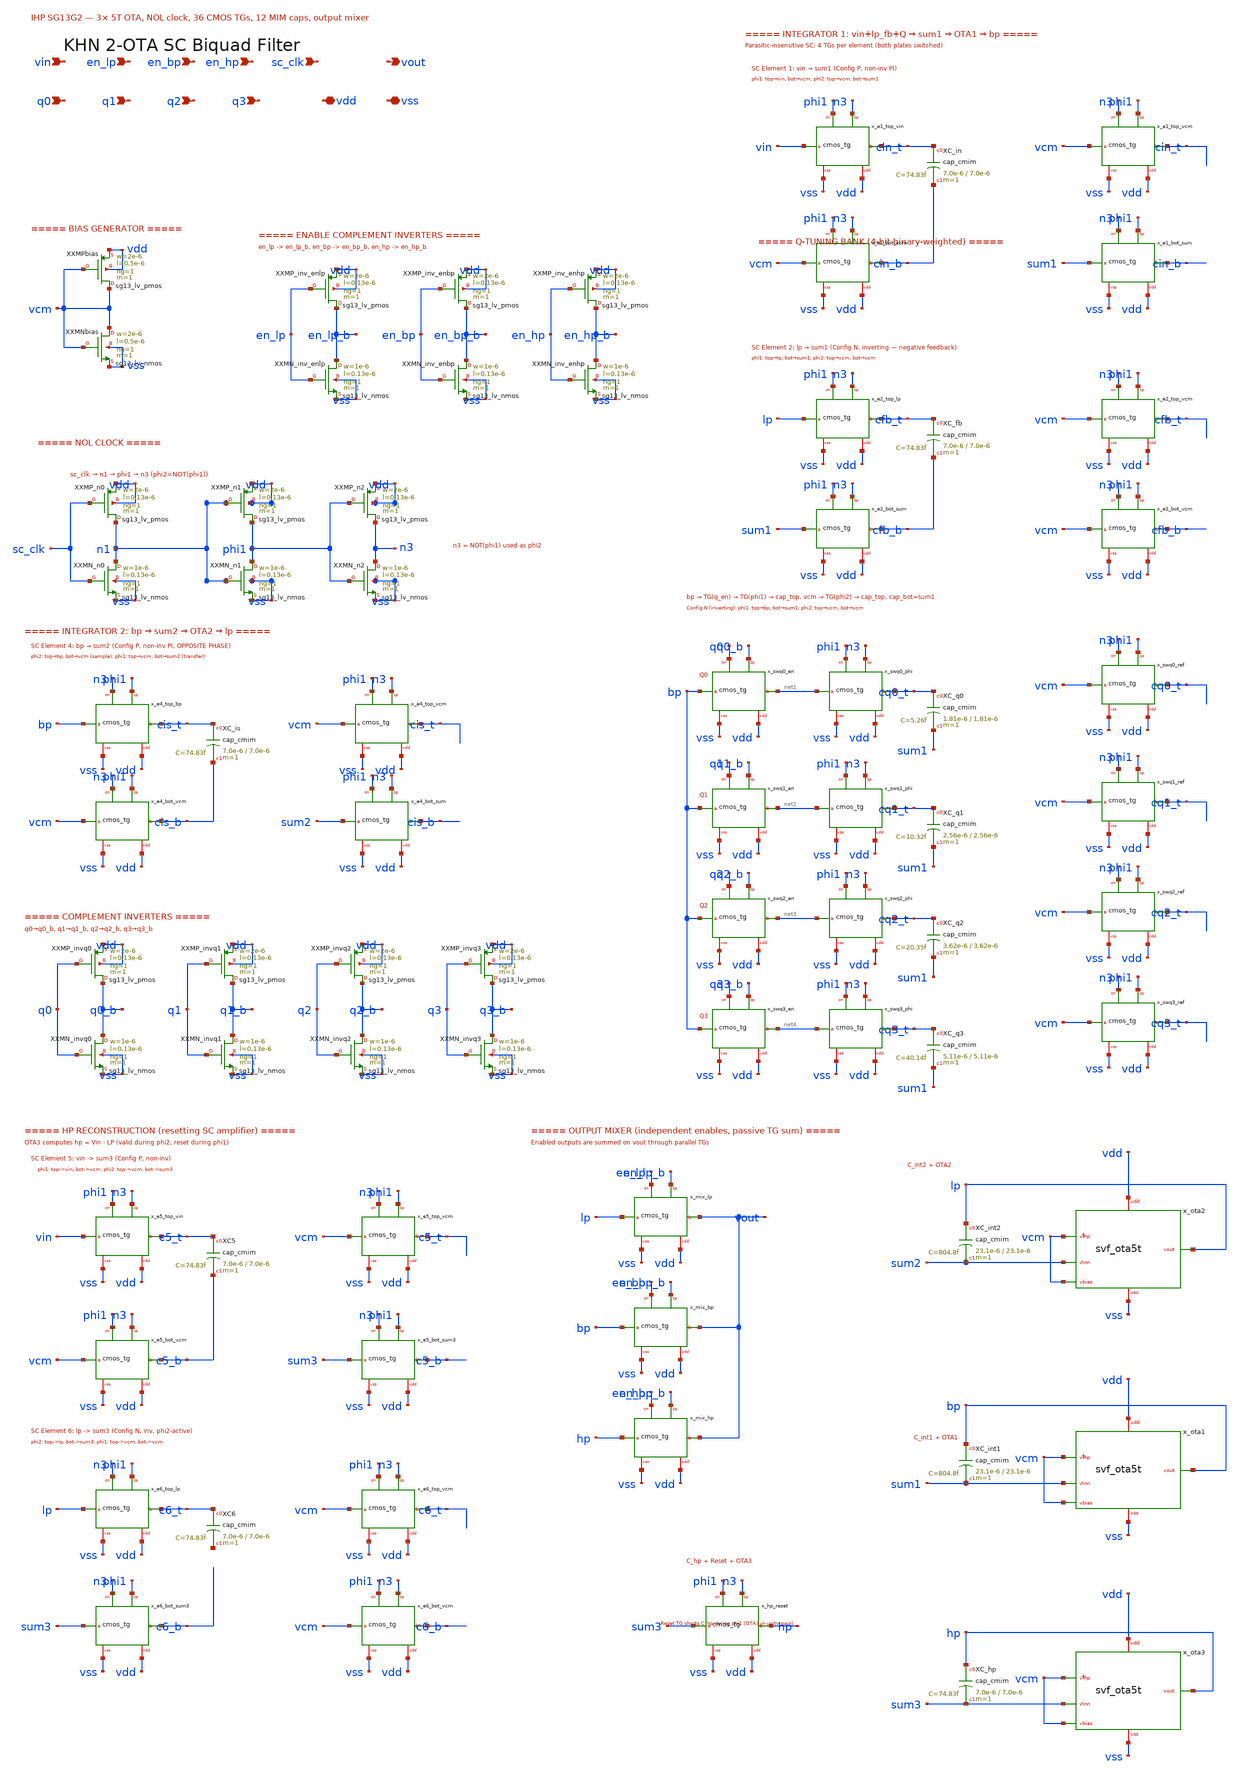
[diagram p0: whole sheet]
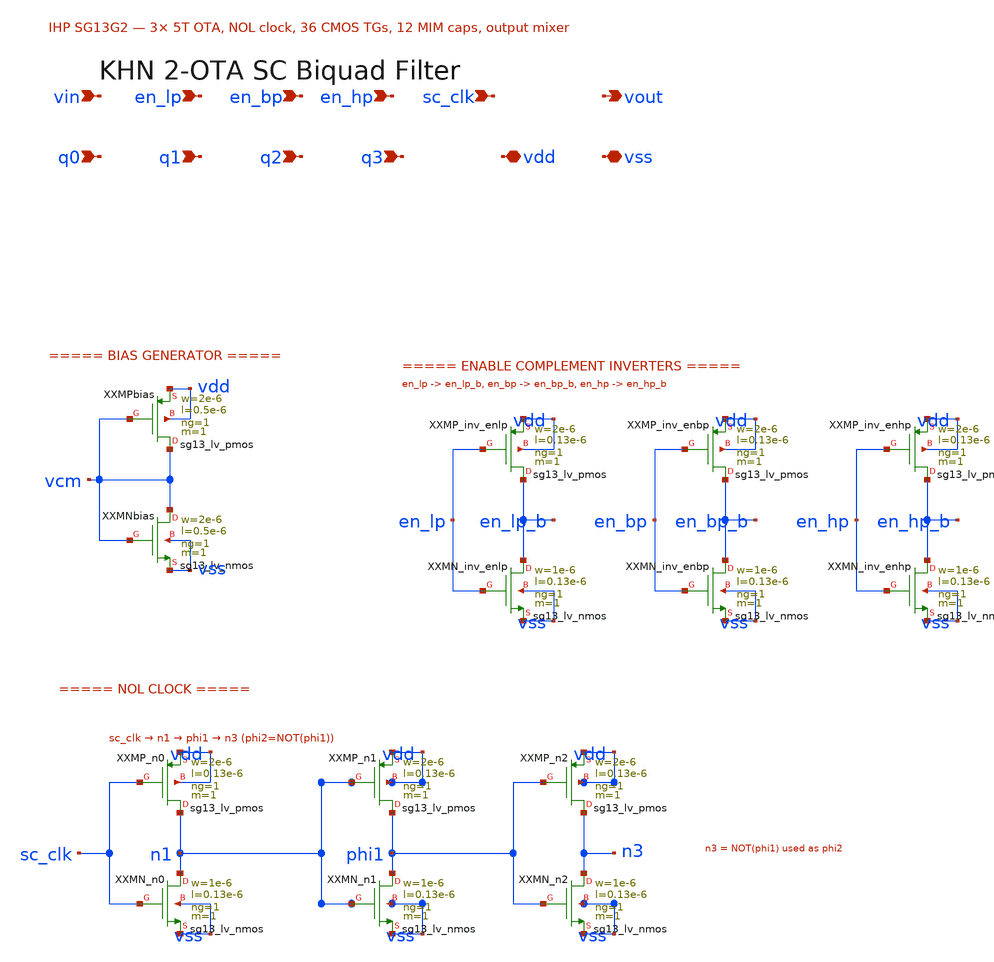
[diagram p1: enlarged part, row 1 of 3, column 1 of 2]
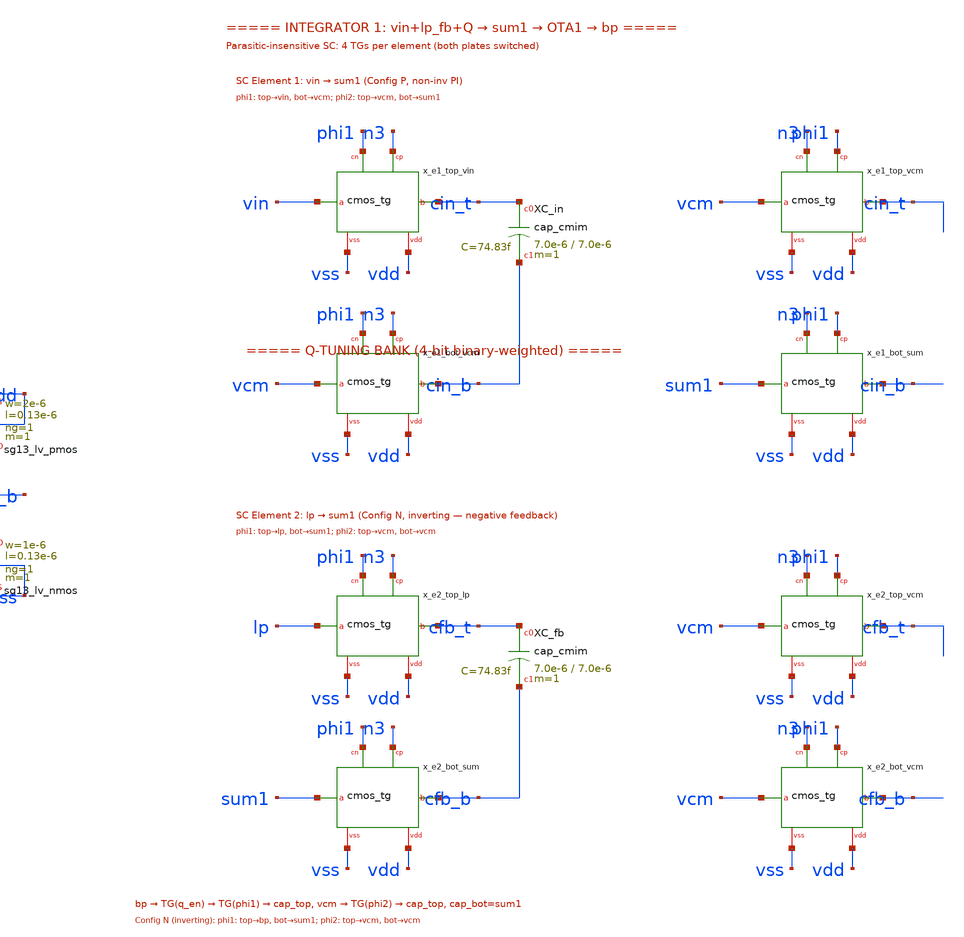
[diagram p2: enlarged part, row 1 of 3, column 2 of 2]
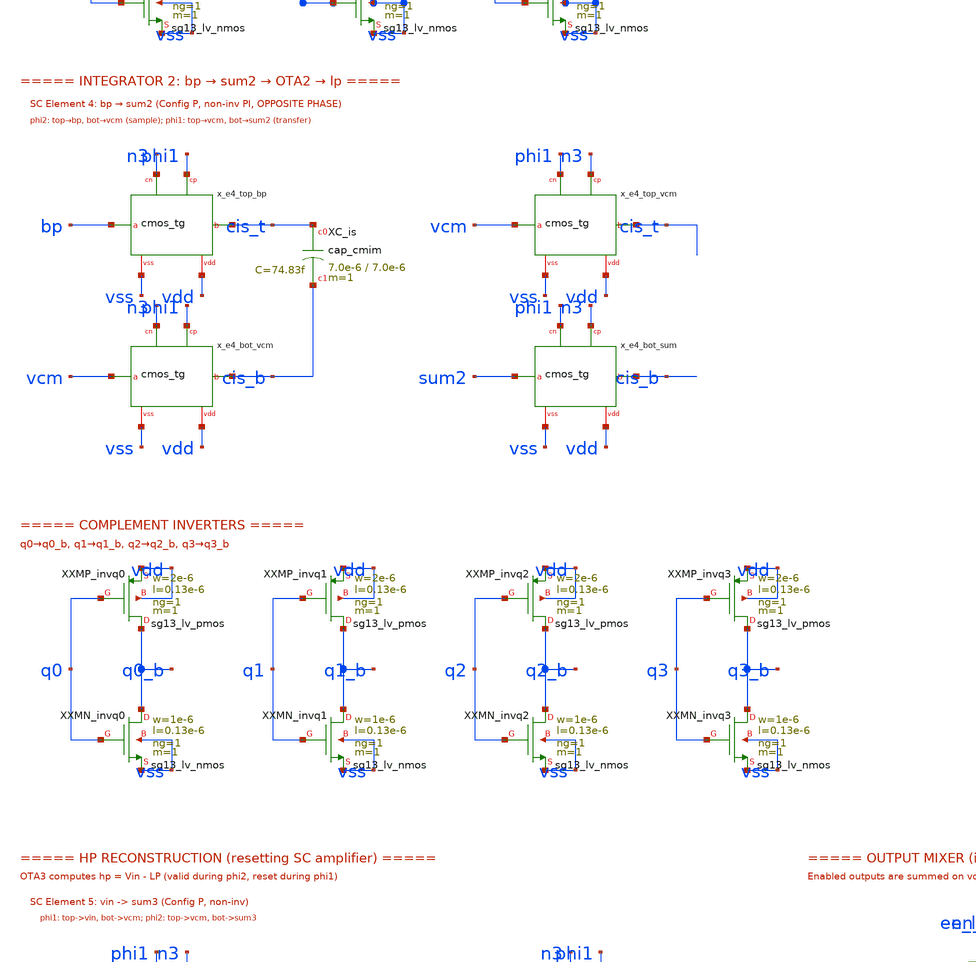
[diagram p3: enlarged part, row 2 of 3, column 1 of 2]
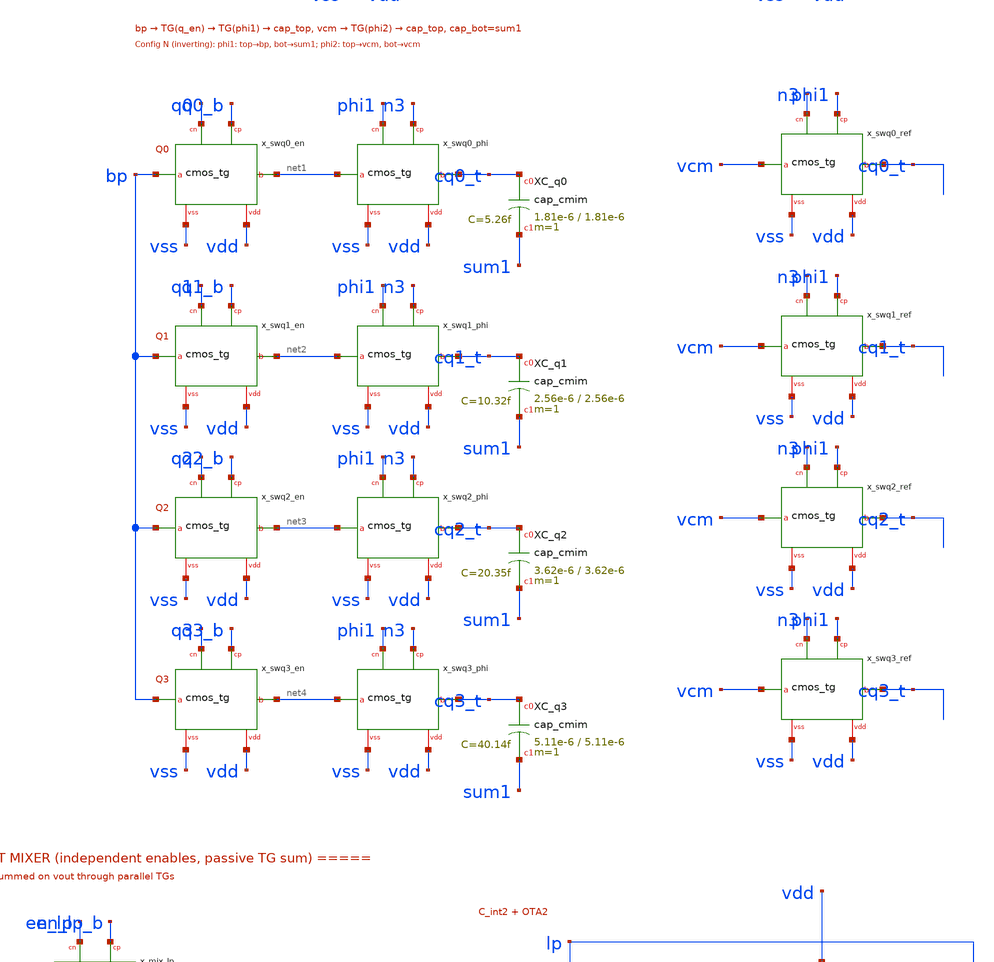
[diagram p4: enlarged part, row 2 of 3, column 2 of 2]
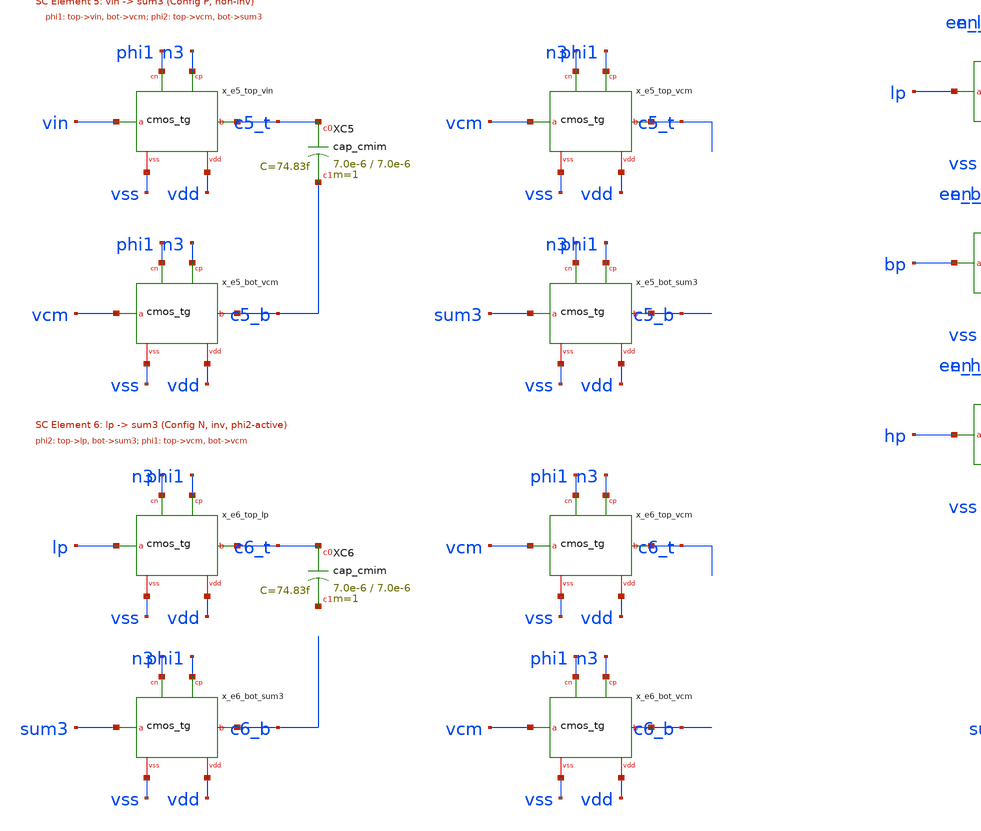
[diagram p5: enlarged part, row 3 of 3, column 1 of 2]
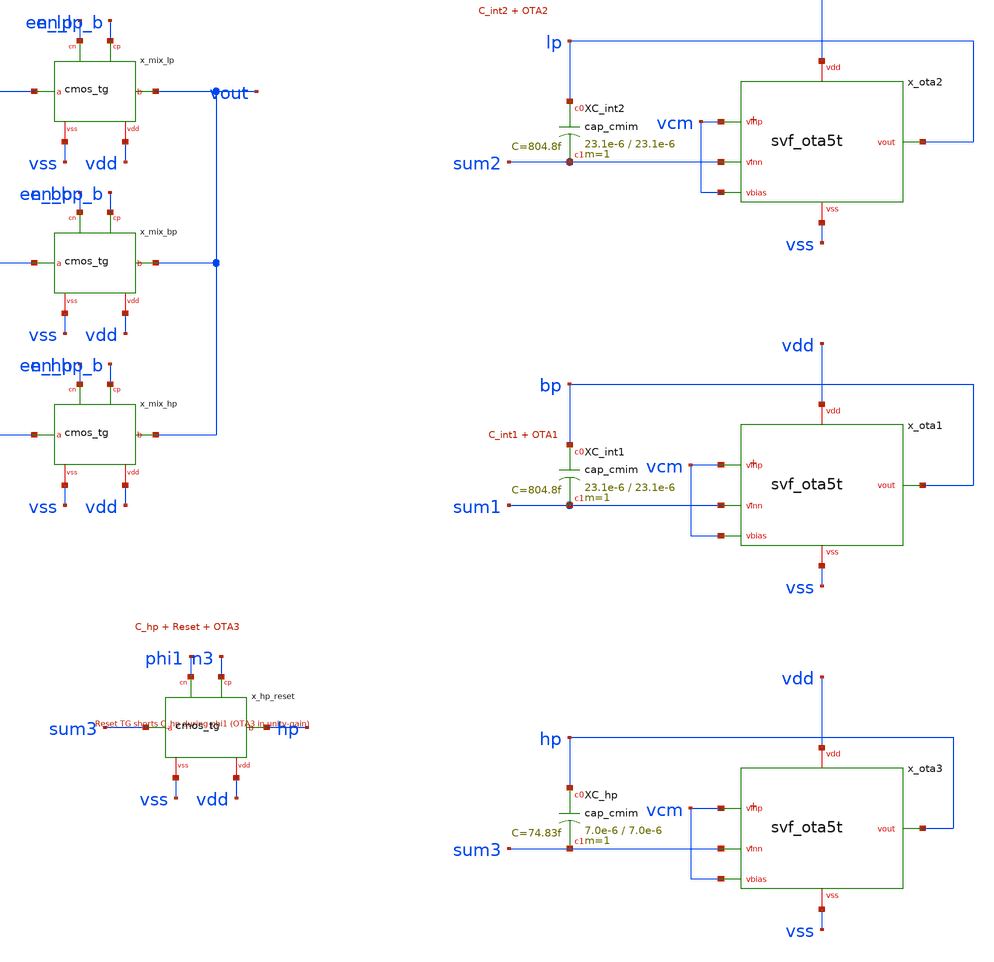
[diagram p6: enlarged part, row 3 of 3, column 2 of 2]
** sch_path: xschem/khn_biquad.sch
**.subckt khn_biquad vin vout en_lp en_bp en_hp sc_clk q0 q1 q2 q3 vdd vss
*.ipin vin
*.opin vout
*.ipin en_lp
*.ipin en_bp
*.ipin en_hp
*.ipin sc_clk
*.ipin q0
*.ipin q1
*.ipin q2
*.ipin q3
*.iopin vdd
*.iopin vss
XXXMPbias vcm vcm vdd vdd sg13_lv_pmos w=2e-6 l=0.5e-6 ng=1 m=1 mm_ok=1
XXXMNbias vcm vcm vss vss sg13_lv_nmos w=2e-6 l=0.5e-6 ng=1 m=1 mm_ok=1
XXXMP_n0 n1 sc_clk vdd vdd sg13_lv_pmos w=2e-6 l=0.13e-6 ng=1 m=1 mm_ok=1
XXXMN_n0 n1 sc_clk vss vss sg13_lv_nmos w=1e-6 l=0.13e-6 ng=1 m=1 mm_ok=1
XXXMP_n1 phi1 n1 vdd vdd sg13_lv_pmos w=2e-6 l=0.13e-6 ng=1 m=1 mm_ok=1
XXXMN_n1 phi1 n1 vss vss sg13_lv_nmos w=1e-6 l=0.13e-6 ng=1 m=1 mm_ok=1
XXXMP_n2 n3 phi1 vdd vdd sg13_lv_pmos w=2e-6 l=0.13e-6 ng=1 m=1 mm_ok=1
XXXMN_n2 n3 phi1 vss vss sg13_lv_nmos w=1e-6 l=0.13e-6 ng=1 m=1 mm_ok=1
x_e1_top_vin vin cin_t phi1 n3 vss vdd cmos_tg
x_e1_bot_vcm vcm cin_b phi1 n3 vss vdd cmos_tg
x_e1_top_vcm vcm cin_t n3 phi1 vss vdd cmos_tg
x_e1_bot_sum sum1 cin_b n3 phi1 vss vdd cmos_tg
XXC_in cin_t cin_b cap_cmim w=7.0e-6 l=7.0e-6 m=1 mm_ok=1
x_e2_top_lp lp cfb_t phi1 n3 vss vdd cmos_tg
x_e2_bot_sum sum1 cfb_b phi1 n3 vss vdd cmos_tg
x_e2_top_vcm vcm cfb_t n3 phi1 vss vdd cmos_tg
x_e2_bot_vcm vcm cfb_b n3 phi1 vss vdd cmos_tg
XXC_fb cfb_t cfb_b cap_cmim w=7.0e-6 l=7.0e-6 m=1 mm_ok=1
XXC_int1 bp sum1 cap_cmim w=23.1e-6 l=23.1e-6 m=1 mm_ok=1
x_ota1 vcm sum1 vcm bp vdd vss svf_ota5t
x_e4_top_bp bp cis_t n3 phi1 vss vdd cmos_tg
x_e4_bot_vcm vcm cis_b n3 phi1 vss vdd cmos_tg
x_e4_top_vcm vcm cis_t phi1 n3 vss vdd cmos_tg
x_e4_bot_sum sum2 cis_b phi1 n3 vss vdd cmos_tg
XXC_is cis_t cis_b cap_cmim w=7.0e-6 l=7.0e-6 m=1 mm_ok=1
XXC_int2 lp sum2 cap_cmim w=23.1e-6 l=23.1e-6 m=1 mm_ok=1
x_ota2 vcm sum2 vcm lp vdd vss svf_ota5t
x_swq0_en bp net1 q0 q0_b vss vdd cmos_tg
x_swq0_phi net1 cq0_t phi1 n3 vss vdd cmos_tg
x_swq0_ref vcm cq0_t n3 phi1 vss vdd cmos_tg
XXC_q0 cq0_t sum1 cap_cmim w=1.81e-6 l=1.81e-6 m=1 mm_ok=1
x_swq1_en bp net2 q1 q1_b vss vdd cmos_tg
x_swq1_phi net2 cq1_t phi1 n3 vss vdd cmos_tg
x_swq1_ref vcm cq1_t n3 phi1 vss vdd cmos_tg
XXC_q1 cq1_t sum1 cap_cmim w=2.56e-6 l=2.56e-6 m=1 mm_ok=1
x_swq2_en bp net3 q2 q2_b vss vdd cmos_tg
x_swq2_phi net3 cq2_t phi1 n3 vss vdd cmos_tg
x_swq2_ref vcm cq2_t n3 phi1 vss vdd cmos_tg
XXC_q2 cq2_t sum1 cap_cmim w=3.62e-6 l=3.62e-6 m=1 mm_ok=1
x_swq3_en bp net4 q3 q3_b vss vdd cmos_tg
x_swq3_phi net4 cq3_t phi1 n3 vss vdd cmos_tg
x_swq3_ref vcm cq3_t n3 phi1 vss vdd cmos_tg
XXC_q3 cq3_t sum1 cap_cmim w=5.11e-6 l=5.11e-6 m=1 mm_ok=1
XXXMP_invq0 q0_b q0 vdd vdd sg13_lv_pmos w=2e-6 l=0.13e-6 ng=1 m=1 mm_ok=1
XXXMN_invq0 q0_b q0 vss vss sg13_lv_nmos w=1e-6 l=0.13e-6 ng=1 m=1 mm_ok=1
XXXMP_invq1 q1_b q1 vdd vdd sg13_lv_pmos w=2e-6 l=0.13e-6 ng=1 m=1 mm_ok=1
XXXMN_invq1 q1_b q1 vss vss sg13_lv_nmos w=1e-6 l=0.13e-6 ng=1 m=1 mm_ok=1
XXXMP_invq2 q2_b q2 vdd vdd sg13_lv_pmos w=2e-6 l=0.13e-6 ng=1 m=1 mm_ok=1
XXXMN_invq2 q2_b q2 vss vss sg13_lv_nmos w=1e-6 l=0.13e-6 ng=1 m=1 mm_ok=1
XXXMP_invq3 q3_b q3 vdd vdd sg13_lv_pmos w=2e-6 l=0.13e-6 ng=1 m=1 mm_ok=1
XXXMN_invq3 q3_b q3 vss vss sg13_lv_nmos w=1e-6 l=0.13e-6 ng=1 m=1 mm_ok=1
x_e5_top_vin vin c5_t phi1 n3 vss vdd cmos_tg
x_e5_bot_vcm vcm c5_b phi1 n3 vss vdd cmos_tg
x_e5_top_vcm vcm c5_t n3 phi1 vss vdd cmos_tg
x_e5_bot_sum3 sum3 c5_b n3 phi1 vss vdd cmos_tg
XXC5 c5_t c5_b cap_cmim w=7.0e-6 l=7.0e-6 m=1 mm_ok=1
x_e6_top_lp lp c6_t n3 phi1 vss vdd cmos_tg
x_e6_bot_sum3 sum3 c6_b n3 phi1 vss vdd cmos_tg
x_e6_top_vcm vcm c6_t phi1 n3 vss vdd cmos_tg
x_e6_bot_vcm vcm c6_b phi1 n3 vss vdd cmos_tg
XXC6 c6_t net5 cap_cmim w=7.0e-6 l=7.0e-6 m=1 mm_ok=1
x_hp_reset sum3 hp phi1 n3 vss vdd cmos_tg
XXC_hp hp sum3 cap_cmim w=7.0e-6 l=7.0e-6 m=1 mm_ok=1
x_ota3 vcm sum3 vcm hp vdd vss svf_ota5t
x_mix_lp lp vout en_lp en_lp_b vss vdd cmos_tg
x_mix_bp bp vout en_bp en_bp_b vss vdd cmos_tg
x_mix_hp hp vout en_hp en_hp_b vss vdd cmos_tg
XXXMP_inv_enlp en_lp_b en_lp vdd vdd sg13_lv_pmos w=2e-6 l=0.13e-6 ng=1 m=1 mm_ok=1
XXXMN_inv_enlp en_lp_b en_lp vss vss sg13_lv_nmos w=1e-6 l=0.13e-6 ng=1 m=1 mm_ok=1
XXXMP_inv_enbp en_bp_b en_bp vdd vdd sg13_lv_pmos w=2e-6 l=0.13e-6 ng=1 m=1 mm_ok=1
XXXMN_inv_enbp en_bp_b en_bp vss vss sg13_lv_nmos w=1e-6 l=0.13e-6 ng=1 m=1 mm_ok=1
XXXMP_inv_enhp en_hp_b en_hp vdd vdd sg13_lv_pmos w=2e-6 l=0.13e-6 ng=1 m=1 mm_ok=1
XXXMN_inv_enhp en_hp_b en_hp vss vss sg13_lv_nmos w=1e-6 l=0.13e-6 ng=1 m=1 mm_ok=1
**.ends

* expanding   symbol:  cmos_tg.sym # of pins=6
** sym_path: xschem/cmos_tg.sym
** sch_path: xschem/cmos_tg.sch
.subckt cmos_tg a b ctrl_n ctrl_p vss vdd
*.iopin a
*.iopin b
*.ipin ctrl_p
*.iopin vss
*.iopin vdd
*.ipin ctrl_n
XXMN a ctrl_n b vss sg13_lv_nmos w=2e-6 l=0.13e-6 ng=1 m=1 mm_ok=1
XXMP b ctrl_p a vdd sg13_lv_pmos w=4e-6 l=0.13e-6 ng=1 m=1 mm_ok=1
.ends


* expanding   symbol:  svf_ota5t.sym # of pins=6
** sym_path: xschem/svf_ota5t.sym
** sch_path: xschem/svf_ota5t.sch
.subckt svf_ota5t vinp vinn vbias vout vdd vss
*.iopin vdd
*.iopin vss
*.ipin vinp
*.ipin vinn
*.opin vout
*.ipin vbias
XXM3 mirr mirr vdd vdd sg13_lv_pmos w=2e-6 l=0.5e-6 ng=1 m=1 mm_ok=1
XXM4 vout mirr vdd vdd sg13_lv_pmos w=2e-6 l=0.5e-6 ng=1 m=1 mm_ok=1
XXM1 mirr vinp tail vss sg13_lv_nmos w=4e-6 l=0.5e-6 ng=1 m=1 mm_ok=1
XXM2 vout vinn tail vss sg13_lv_nmos w=4e-6 l=0.5e-6 ng=1 m=1 mm_ok=1
XXM5 tail vbias vss vss sg13_lv_nmos w=2e-6 l=0.5e-6 ng=1 m=1 mm_ok=1
.ends

.end
